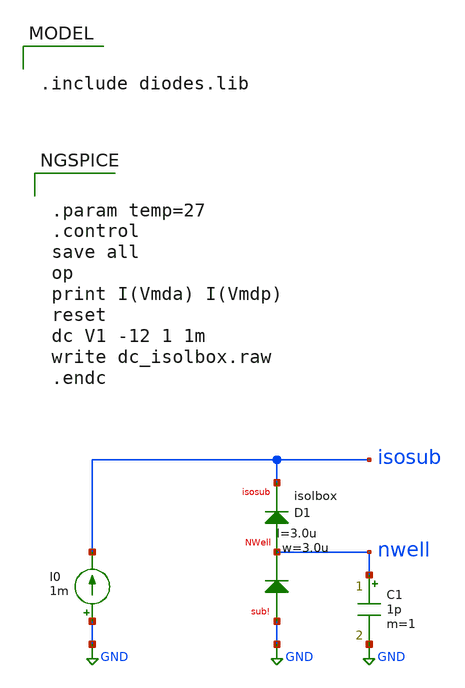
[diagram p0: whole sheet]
** sch_path: ihp-sg13g2/libs.tech/xschem/sg13g2_tests/dc_isolbox.sch
* Copyright 2023 IHP PDK Authors
**.subckt dc_isolbox
I0 GND isosub 1m
C1 nwell GND 1p m=1
XD1 nwell isosub GND isolbox l=3.0u w=3.0u
**** begin user architecture code

.include diodes.lib



.param temp=27
.control
save all
op
print I(Vmda) I(Vmdp)
reset
dc V1 -12 1 1m
write dc_isolbox.raw
.endc


**** end user architecture code
**.ends
.GLOBAL GND
.end
